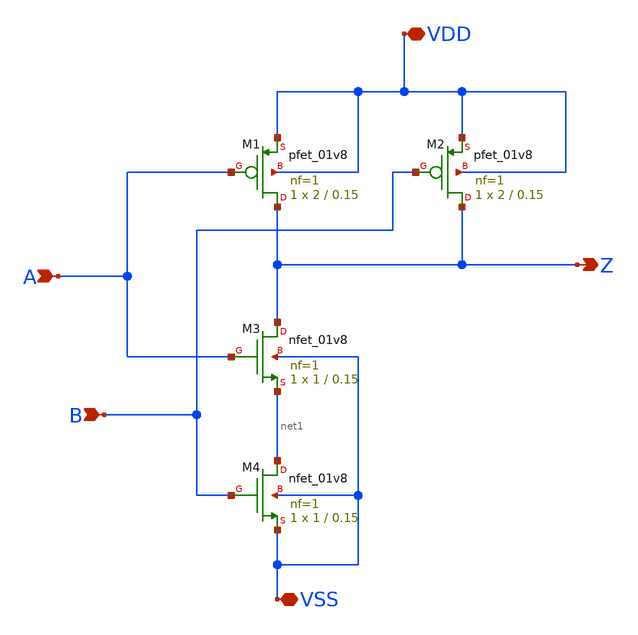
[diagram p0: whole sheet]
** sch_path: NAND1.sch
**.subckt NAND1 A B VDD VSS Z
*.ipin A
*.ipin B
*.iopin VDD
*.iopin VSS
*.opin Z
XM1 Z A VDD VDD sky130_fd_pr__pfet_01v8 L=0.15 W=2 nf=1 ad='int((1 + 1)/2) * 2 / 1 * 0.29' as='int((1 + 2)/2) * 2 / 1 * 0.29'
+ pd='2*int((1 + 1)/2) * (2 / 1 + 0.29)' ps='2*int((1 + 2)/2) * (2 / 1 + 0.29)' nrd='0.29 / 2 ' nrs='0.29 / 2 '
+ sa=0 sb=0 sd=0 mult=1 m=1
XM2 Z B VDD VDD sky130_fd_pr__pfet_01v8 L=0.15 W=2 nf=1 ad='int((1 + 1)/2) * 2 / 1 * 0.29' as='int((1 + 2)/2) * 2 / 1 * 0.29'
+ pd='2*int((1 + 1)/2) * (2 / 1 + 0.29)' ps='2*int((1 + 2)/2) * (2 / 1 + 0.29)' nrd='0.29 / 2 ' nrs='0.29 / 2 '
+ sa=0 sb=0 sd=0 mult=1 m=1
XM3 Z A net1 VSS sky130_fd_pr__nfet_01v8 L=0.15 W=1 nf=1 ad='int((1 + 1)/2) * 1 / 1 * 0.29' as='int((1 + 2)/2) * 1 / 1 * 0.29'
+ pd='2*int((1 + 1)/2) * (1 / 1 + 0.29)' ps='2*int((1 + 2)/2) * (1 / 1 + 0.29)' nrd='0.29 / 1 ' nrs='0.29 / 1 '
+ sa=0 sb=0 sd=0 mult=1 m=1
XM4 net1 B VSS VSS sky130_fd_pr__nfet_01v8 L=0.15 W=1 nf=1 ad='int((1 + 1)/2) * 1 / 1 * 0.29' as='int((1 + 2)/2) * 1 / 1 * 0.29'
+ pd='2*int((1 + 1)/2) * (1 / 1 + 0.29)' ps='2*int((1 + 2)/2) * (1 / 1 + 0.29)' nrd='0.29 / 1 ' nrs='0.29 / 1 '
+ sa=0 sb=0 sd=0 mult=1 m=1
**.ends
.end
